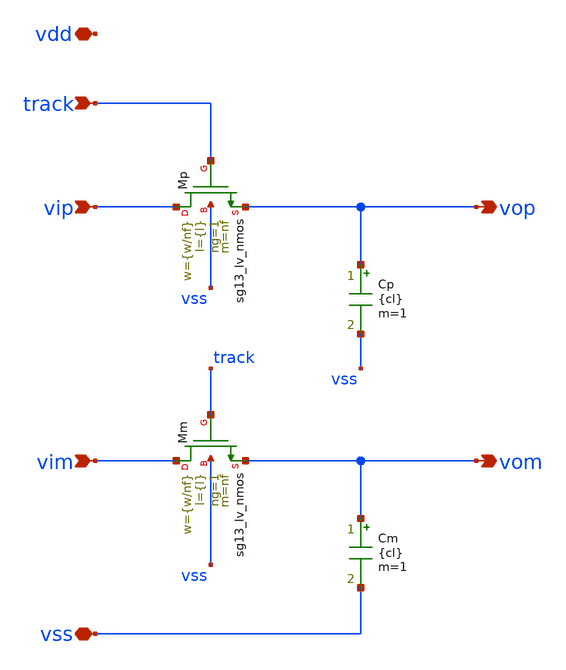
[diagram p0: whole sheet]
** sch_path: old/xschem/th_nmos.sch
**.subckt th_nmos vip vop vim vom track vss vdd
*.ipin vip
*.opin vop
*.ipin vim
*.opin vom
*.ipin track
*.iopin vss
*.iopin vdd
XMp vip track vop vss sg13_lv_nmos w={w/nf} l={l} ng=1 m=nf mm_ok=1
Cp vop vss {cl} m=1
XMm vim track vom vss sg13_lv_nmos w={w/nf} l={l} ng=1 m=nf mm_ok=1
Cm vom vss {cl} m=1
**.ends
.end
